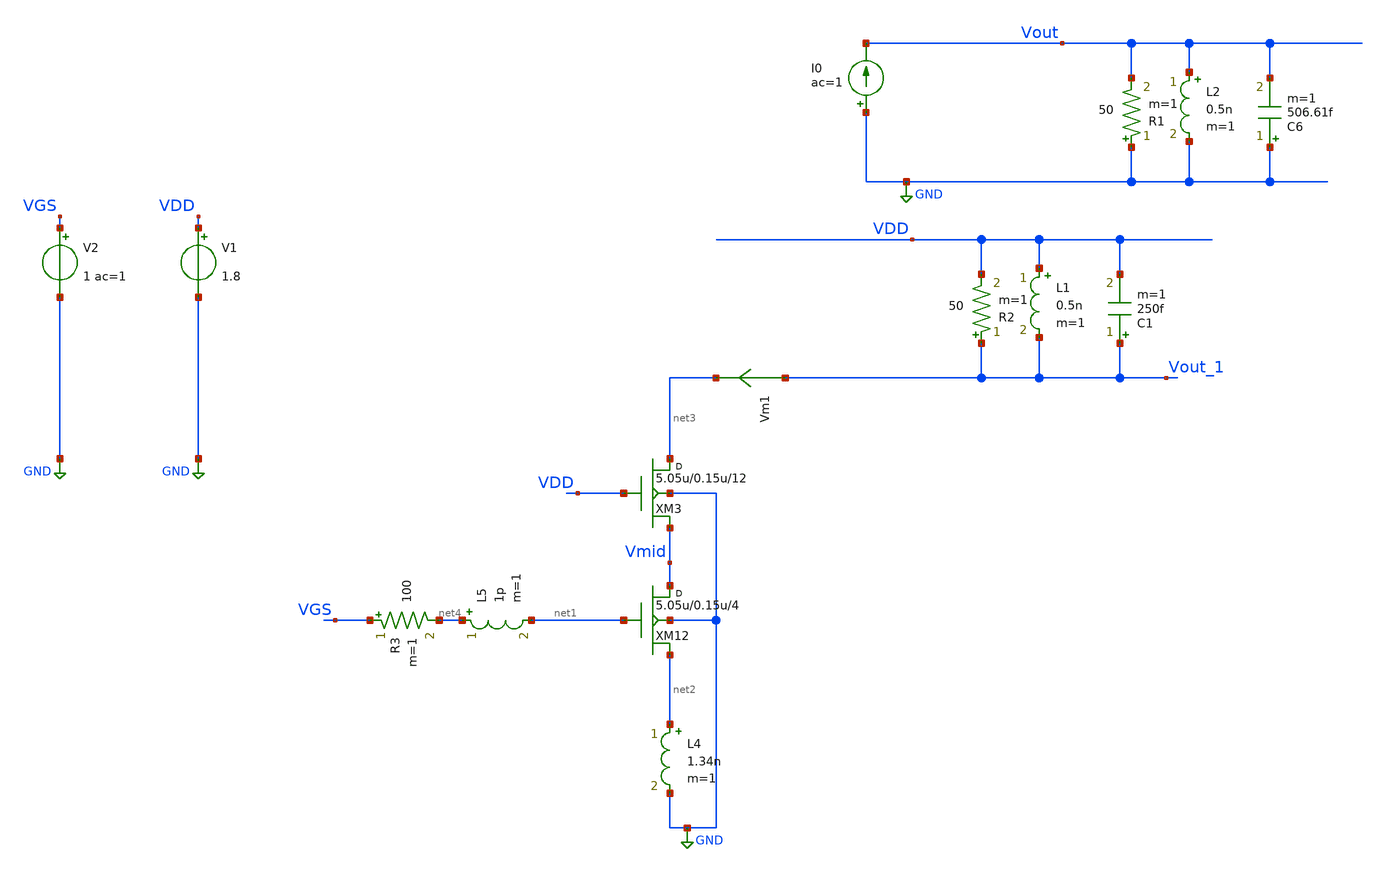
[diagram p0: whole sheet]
** sch_path: xschem/lna/Input_10G.sch
**.subckt Input_10G
I0 GND Vout ac=1
L2 Vout GND 0.5n m=1
C6 GND Vout 506.61f m=1
R1 GND Vout 50 m=1
XM12 Vmid net1 net2 GND sky130_fd_pr__rf_nfet_01v8_bM04W5p00L0p15_ext w=5.05u l=0.15u m=4
L1 VDD Vout_1 0.5n m=1
C1 Vout_1 VDD 250f m=1
R2 Vout_1 VDD 50 m=1
V1 VDD GND 1.8
V2 VGS GND 1 ac=1
XM3 net3 VDD Vmid GND sky130_fd_pr__rf_nfet_01v8_bM04W5p00L0p15_ext w=5.05u l=0.15u m=12
Vm1 Vout_1 net3 0
.save i(vm1)
R3 VGS net4 100 m=1
L4 net2 GND 1.34n m=1
L5 net4 net1 1p m=1
**** begin user architecture code


.subckt sky130_fd_pr__rf_nfet_01v8_bM04W5p00L0p15_ext DRAIN GATE SOURCE SUBSTRATE
X0 DRAIN GATE SOURCE SUBSTRATE sky130_fd_pr__nfet_01v8 ad=2.828e+12p pd=2.132e+07u as=4.242e+12p
+ ps=3.198e+07u w=5.05e+06u l=150000u
X1 SOURCE SUBSTRATE SUBSTRATE SUBSTRATE sky130_fd_pr__nfet_01v8 ad=0p pd=0u as=3.03e+12p
+ ps=2.14e+07u w=5.05e+06u l=150000u
X2 SOURCE GATE DRAIN SUBSTRATE sky130_fd_pr__nfet_01v8 ad=0p pd=0u as=0p ps=0u w=5.05e+06u l=150000u
X3 DRAIN GATE SOURCE SUBSTRATE sky130_fd_pr__nfet_01v8 ad=0p pd=0u as=0p ps=0u w=5.05e+06u l=150000u
X4 SUBSTRATE SUBSTRATE SOURCE SUBSTRATE sky130_fd_pr__nfet_01v8 ad=0p pd=0u as=0p ps=0u w=5.05e+06u
+ l=150000u
X5 SOURCE GATE DRAIN SUBSTRATE sky130_fd_pr__nfet_01v8 ad=0p pd=0u as=0p ps=0u w=5.05e+06u l=150000u
.ends
*.sp dec 1000 0.1e9 100e9 1
*.ac dec 1000 0.01e9 100e9
.option GMIN=1e-15
.control
save all
run
display

ac dec 10 1G 100G

plot Vout
plot abs(real(Vout))
plot imag(Vout)

plot Vout_1
plot abs(real(Vout_1))
plot imag(Vout_1)
plot vm1#branch

.endc



** opencircuitdesign pdks install
.lib $::SKYWATER_MODELS/sky130.lib.spice tt


**** end user architecture code
**.ends
.GLOBAL GND
.end
